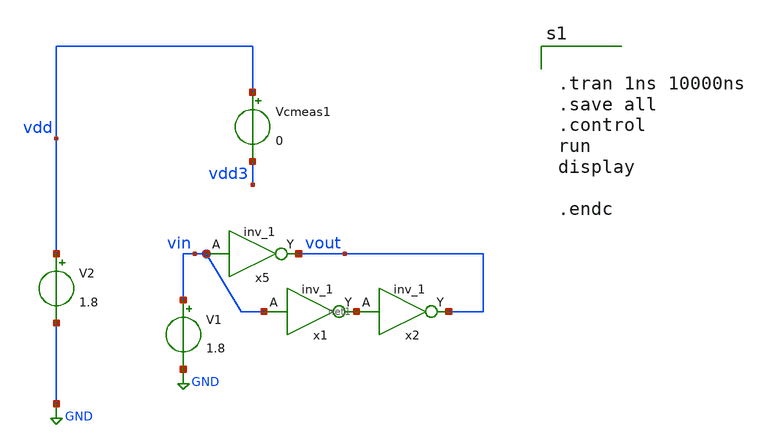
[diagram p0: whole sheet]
** sch_path: xschem/cptest.sch
**.subckt cptest
x5 vin gnd gnd vdd3 vdd3 vout sky130_fd_sc_hd__inv_1
V2 vdd GND 1.8
Vcmeas1 vdd vdd3 0
x1 vin gnd gnd vdd3 vdd3 net1 sky130_fd_sc_hd__inv_1
x2 net1 gnd gnd vdd3 vdd3 vout sky130_fd_sc_hd__inv_1
V1 vin GND 1.8
**** begin user architecture code
.lib $::SKYWATER_MODELS/sky130.lib.spice tt
.include $::PDKPATH/libs.ref/sky130_fd_sc_hd/spice/sky130_fd_sc_hd.spice


.tran 1ns 10000ns
.save all
.control
run
display

.endc


**** end user architecture code
**.ends
.GLOBAL GND
.end
